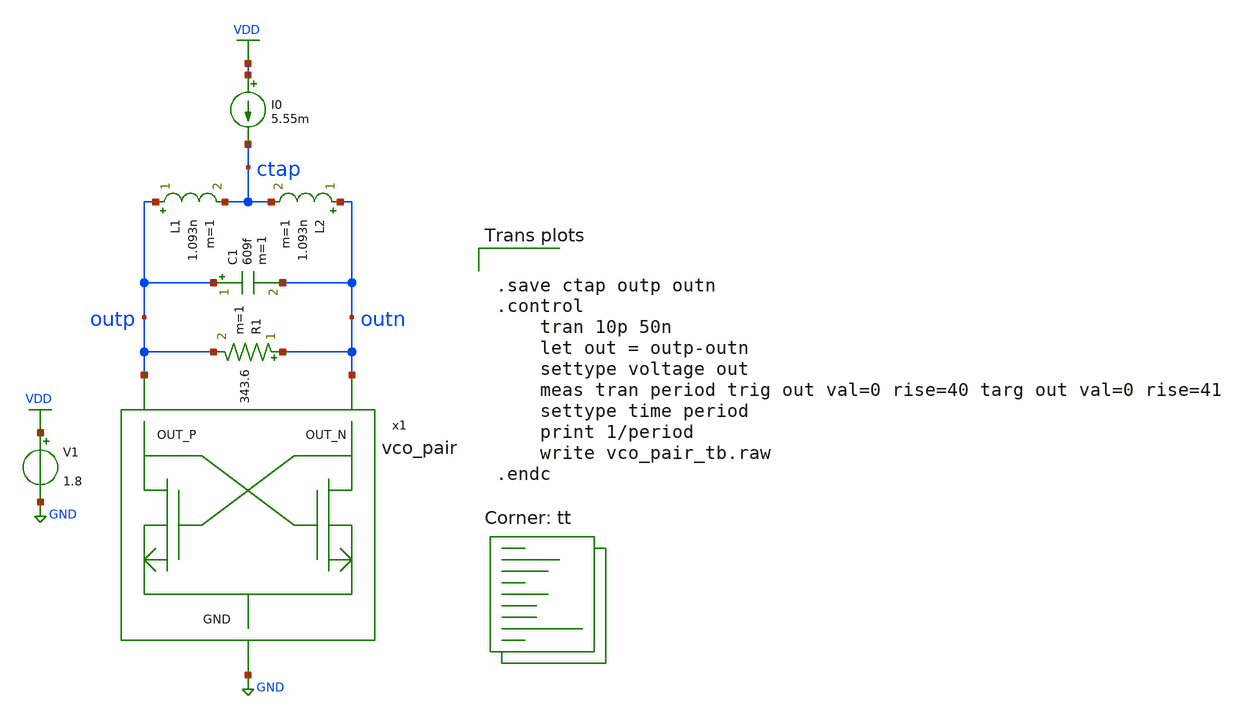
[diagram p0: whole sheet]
** sch_path: xschem/vco/testbenches/vco_pair/pex/vco_pair_tb.sch
* YI/C9Shc8z/CWPKLJb8BQD+O4ziO4wpAwbu7u7s7HEAy2IIt2IIlQD6O4ziO4ypAAICtDl/GPL8AgNZy7Go7vwAAAAAAAAAAAAAAAAAAAAAAAPeMn2NHvywNosQhFFq
**.subckt vco_pair_tb
x1 outp outn GND vco_pair
R1 outn outp 343.6 m=1
C1 outp outn 609f m=1
L1 outp ctap 1.093n m=1
L2 outn ctap 1.093n m=1
I0 VDD ctap 5.55m
V1 VDD GND 1.8
**** begin user architecture code


.save ctap outp outn
.control
    tran 10p 50n
    let out = outp-outn
    settype voltage out
    meas tran period trig out val=0 rise=40 targ out val=0 rise=41
    settype time period
    print 1/period
    write vco_pair_tb.raw
.endc


.lib $::SKYWATER_MODELS/sky130.lib.spice tt
**** end user architecture code
**.ends
.GLOBAL VDD
.GLOBAL GND
.end
